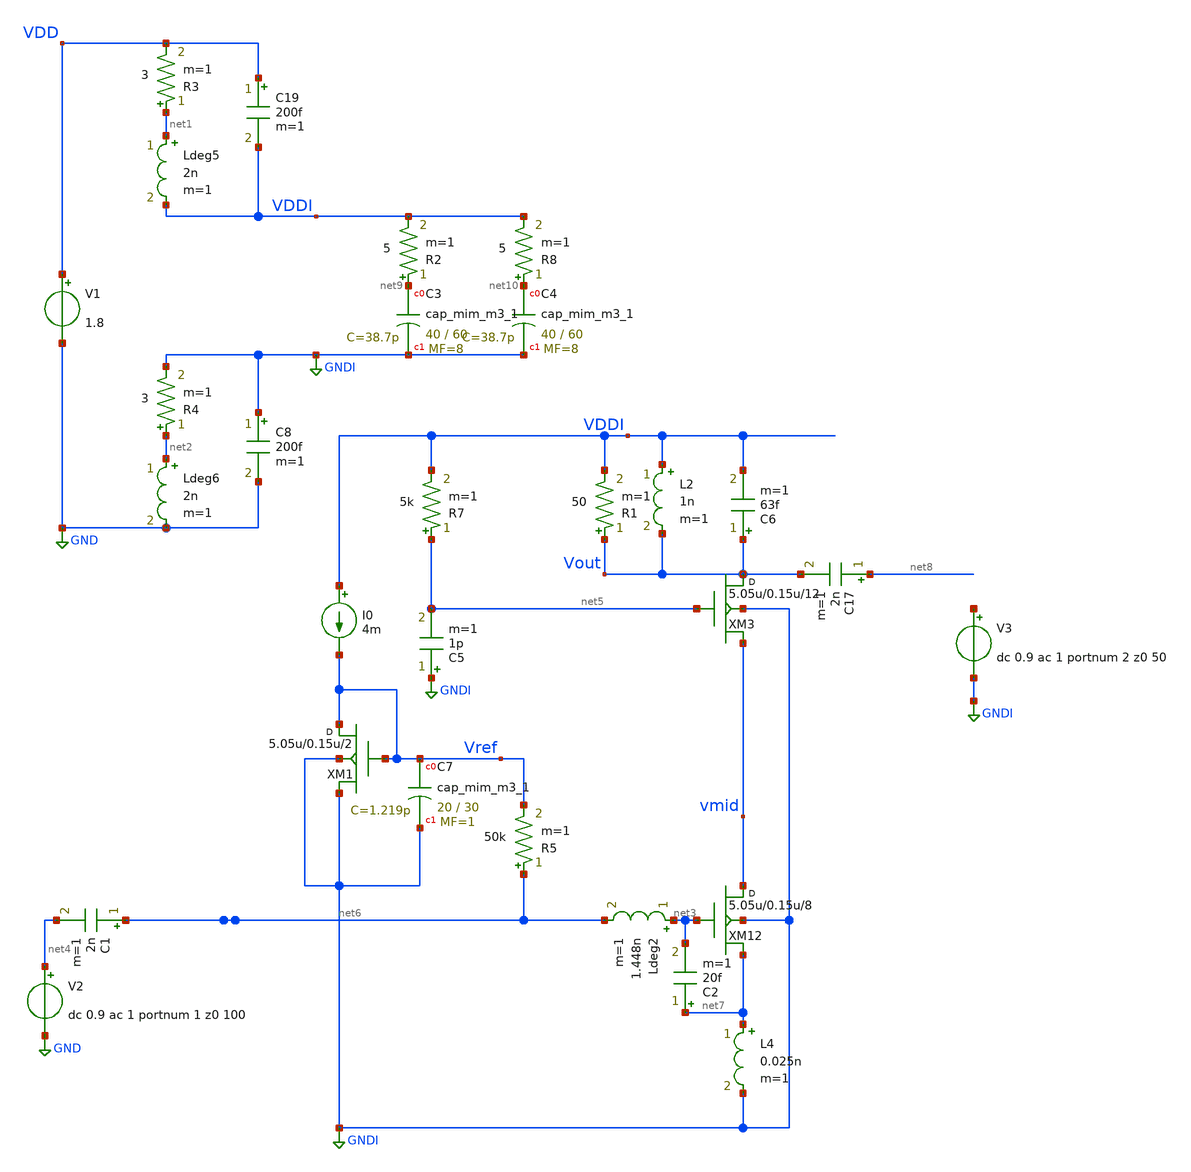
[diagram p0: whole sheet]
** sch_path: xschem/lna/15G_LNA.sch
**.subckt 15G_LNA
V1 VDD GND 1.8
V2 net4 GND dc 0.9 ac 1 portnum 1 z0 100
I0 VDDI Vref 4m
XM1 Vref Vref GNDI GNDI sky130_fd_pr__rf_nfet_01v8_bM04W5p00L0p15_ext w=5.05u l=0.15u m=2
XC7 Vref GNDI sky130_fd_pr__cap_mim_m3_1 W=20 L=30 MF=1 m=1
Ldeg5 net1 VDDI 2n m=1
R3 net1 VDD 3 m=1
Ldeg6 net2 GND 2n m=1
R4 net2 GNDI 3 m=1
XM12 vmid net3 net7 GNDI sky130_fd_pr__rf_nfet_01v8_bM04W5p00L0p15_ext w=5.05u l=0.15u m=8
C17 net8 Vout 2n m=1
L2 VDDI Vout 1n m=1
XC3 net9 GNDI sky130_fd_pr__cap_mim_m3_1 W=40 L=60 MF=8 m=8
C8 GNDI GND 200f m=1
C19 VDD VDDI 200f m=1
R2 net9 VDDI 5 m=1
R5 net6 Vref 50k m=1
C1 net6 net4 2n m=1
C6 Vout VDDI 63f m=1
XM3 Vout net5 vmid GNDI sky130_fd_pr__rf_nfet_01v8_bM04W5p00L0p15_ext w=5.05u l=0.15u m=12
Ldeg2 net3 net6 1.448n m=1
XC4 net10 GNDI sky130_fd_pr__cap_mim_m3_1 W=40 L=60 MF=8 m=8
R8 net10 VDDI 5 m=1
L4 net7 GNDI 0.025n m=1
V3 net11 GNDI dc 0.9 ac 1 portnum 2 z0 50
R7 net5 VDDI 5k m=1
C5 GNDI net5 1p m=1
C2 net7 net3 20f m=1
R1 Vout VDDI 50 m=1
**** begin user architecture code


.subckt sky130_fd_pr__rf_nfet_01v8_bM04W5p00L0p15_ext DRAIN GATE SOURCE SUBSTRATE
X0 DRAIN GATE SOURCE SUBSTRATE sky130_fd_pr__nfet_01v8 ad=2.828e+12p pd=2.132e+07u as=4.242e+12p
+ ps=3.198e+07u w=5.05e+06u l=150000u
X1 SOURCE SUBSTRATE SUBSTRATE SUBSTRATE sky130_fd_pr__nfet_01v8 ad=0p pd=0u as=3.03e+12p
+ ps=2.14e+07u w=5.05e+06u l=150000u
X2 SOURCE GATE DRAIN SUBSTRATE sky130_fd_pr__nfet_01v8 ad=0p pd=0u as=0p ps=0u w=5.05e+06u l=150000u
X3 DRAIN GATE SOURCE SUBSTRATE sky130_fd_pr__nfet_01v8 ad=0p pd=0u as=0p ps=0u w=5.05e+06u l=150000u
X4 SUBSTRATE SUBSTRATE SOURCE SUBSTRATE sky130_fd_pr__nfet_01v8 ad=0p pd=0u as=0p ps=0u w=5.05e+06u
+ l=150000u
X5 SOURCE GATE DRAIN SUBSTRATE sky130_fd_pr__nfet_01v8 ad=0p pd=0u as=0p ps=0u w=5.05e+06u l=150000u
.ends
.sp dec 1000 0.1e9 100e9 1
*.ac dec 1000 0.01e9 100e9
.control
save all
run
display
let z11=50*(1+s_1_1)/(1-s_1_1)
let z22=50*(1+s_2_2)/(1-s_2_2)
let S11 = S_1_1
let S21 = S_2_1
let S12 = S_1_2
let S22 = S_2_2

* Stability
let delta=S11*S22-S12*S21
let K    = (1-mag(S11)^2-mag(S22)^2+mag(delta)^2)/(2*mag(S12*S21))
let mu   = (1-mag(S11)^2)/(mag(S22-conj(S11)*delta)+mag(S21*S12))
plot real(z11) real(z22)
plot imag(z11) imag(z22)
plot db(mag(S_1_1)) db(mag(S_2_2)) db(mag(S_2_1))

plot db(K)
plot mag(delta)
plot db(mu)
plot NF NFmin
.endc



** opencircuitdesign pdks install
.lib $::SKYWATER_MODELS/sky130.lib.spice tt


**** end user architecture code
**.ends
.GLOBAL GND
.GLOBAL GNDI
.end
